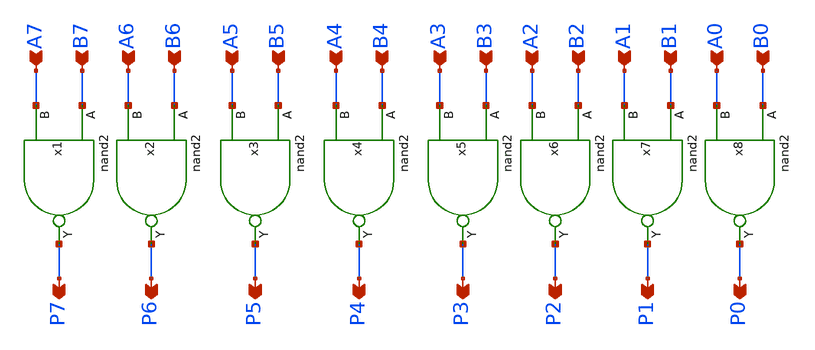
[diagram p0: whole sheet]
** sch_path: design/xschem/NAND/nand_8_bitwise.sch
**.subckt nand_8_bitwise B7 B5 B6 B4 B3 B2 B1 B0 P7 P6 P5 P4 P3 P2 P1 P0 A7 A5 A6 A4 A3 A2 A1 A0
*.ipin B7
*.ipin B5
*.ipin B6
*.ipin B4
*.ipin B3
*.ipin B2
*.ipin B1
*.ipin B0
*.opin P7
*.opin P6
*.opin P5
*.opin P4
*.opin P3
*.opin P2
*.opin P1
*.opin P0
*.ipin A7
*.ipin A5
*.ipin A6
*.ipin A4
*.ipin A3
*.ipin A2
*.ipin A1
*.ipin A0
x1 B7 A7 VSS VDD P7 nand2
x2 B6 A6 VSS VDD P6 nand2
x3 B5 A5 VSS VDD P5 nand2
x4 B4 A4 VSS VDD P4 nand2
x5 B3 A3 VSS VDD P3 nand2
x6 B2 A2 VSS VDD P2 nand2
x7 B1 A1 VSS VDD P1 nand2
x8 B0 A0 VSS VDD P0 nand2
**.ends

* expanding   symbol:  NAND/nand2.sym # of pins=3
** sym_path: design/xschem/NAND/nand2.sym
** sch_path: design/xschem/NAND/nand2.sch
.subckt nand2 A B VSS VDD Y
*.ipin A
*.opin Y
*.ipin B
XM1 Y A VDD VDD sky130_fd_pr__pfet_01v8 L=0.15 W=3.2 nf=1 ad='int((nf+1)/2) * W/nf * 0.29' as='int((nf+2)/2) * W/nf * 0.29'
+ pd='2*int((nf+1)/2) * (W/nf + 0.29)' ps='2*int((nf+2)/2) * (W/nf + 0.29)' nrd='0.29 / W' nrs='0.29 / W'
+ sa=0 sb=0 sd=0 mult=1 m=1
XM2 Y A net1 net1 sky130_fd_pr__nfet_01v8 L=0.15 W=2 nf=1 ad='int((nf+1)/2) * W/nf * 0.29' as='int((nf+2)/2) * W/nf * 0.29'
+ pd='2*int((nf+1)/2) * (W/nf + 0.29)' ps='2*int((nf+2)/2) * (W/nf + 0.29)' nrd='0.29 / W' nrs='0.29 / W'
+ sa=0 sb=0 sd=0 mult=1 m=1
XM3 net1 B VSS VSS sky130_fd_pr__nfet_01v8 L=0.15 W=2 nf=1 ad='int((nf+1)/2) * W/nf * 0.29' as='int((nf+2)/2) * W/nf * 0.29'
+ pd='2*int((nf+1)/2) * (W/nf + 0.29)' ps='2*int((nf+2)/2) * (W/nf + 0.29)' nrd='0.29 / W' nrs='0.29 / W'
+ sa=0 sb=0 sd=0 mult=1 m=1
XM4 Y B VDD VDD sky130_fd_pr__pfet_01v8 L=0.15 W=3.2 nf=1 ad='int((nf+1)/2) * W/nf * 0.29' as='int((nf+2)/2) * W/nf * 0.29'
+ pd='2*int((nf+1)/2) * (W/nf + 0.29)' ps='2*int((nf+2)/2) * (W/nf + 0.29)' nrd='0.29 / W' nrs='0.29 / W'
+ sa=0 sb=0 sd=0 mult=1 m=1
.ends

.end
